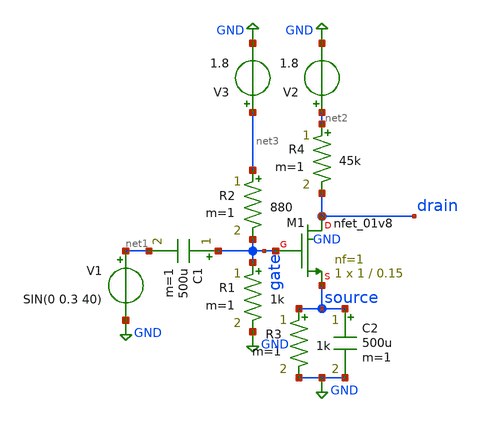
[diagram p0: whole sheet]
** sch_path: xschem/lownoiseamplifier/cs-exper.sch
**.subckt cs-exper
XM1 drain gate source GND sky130_fd_pr__nfet_01v8 L=0.15 W=1 nf=1 ad='int((nf+1)/2) * W/nf * 0.29' as='int((nf+2)/2) * W/nf * 0.29'
+ pd='2*int((nf+1)/2) * (W/nf + 0.29)' ps='2*int((nf+2)/2) * (W/nf + 0.29)' nrd='0.29 / W' nrs='0.29 / W'
+ sa=0 sb=0 sd=0 mult=1 m=1
V1 net1 GND SIN(0 0.3 40)
C1 gate net1 500u m=1
R1 gate GND 1k m=1
R2 net3 gate 880 m=1
R3 source GND 1k m=1
R4 net2 drain 45k m=1
V2 net2 GND 1.8
V3 net3 GND 1.8
C2 source GND 500u m=1
**** begin user architecture code
 ** manual skywater pdks install (with patches applied)
* .lib $::SKYWATER_MODELS/models/sky130.lib.spice tt

** opencircuitdesign pdks install
.lib $::SKYWATER_MODELS/sky130.lib.spice tt

.param mc_mm_switch=0
.param mc_pr_switch=0



.tran 0.001s 0.1s
.control
  run
  plot v(drain) v(gate) v(source)
  plot -i(v2)
.endc
.save all


**** end user architecture code
**.ends
.GLOBAL GND
.end
